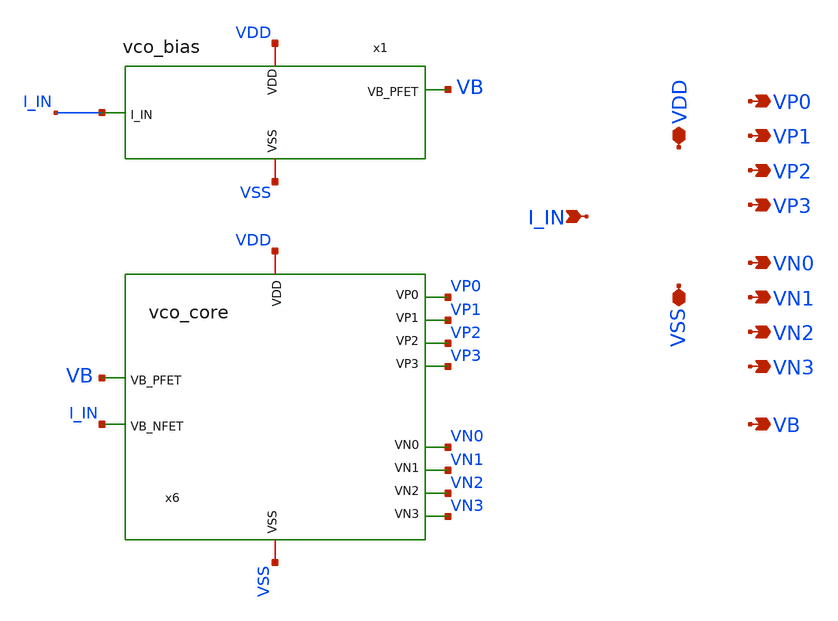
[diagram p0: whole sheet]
** sch_path: xschem/vco.sch
**.subckt vco VDD VSS I_IN VP0 VP1 VP2 VP3 VN0 VN1 VN2 VN3 VB
*.iopin VDD
*.iopin VSS
*.ipin I_IN
*.opin VP0
*.opin VP1
*.opin VP2
*.opin VP3
*.opin VN0
*.opin VN1
*.opin VN2
*.opin VN3
*.opin VB
x1 VDD VSS I_IN VB vco_bias
x6 VDD VSS VB I_IN VP0 VP1 VP2 VP3 VN0 VN1 VN2 VN3 vco_core
**.ends
.end
